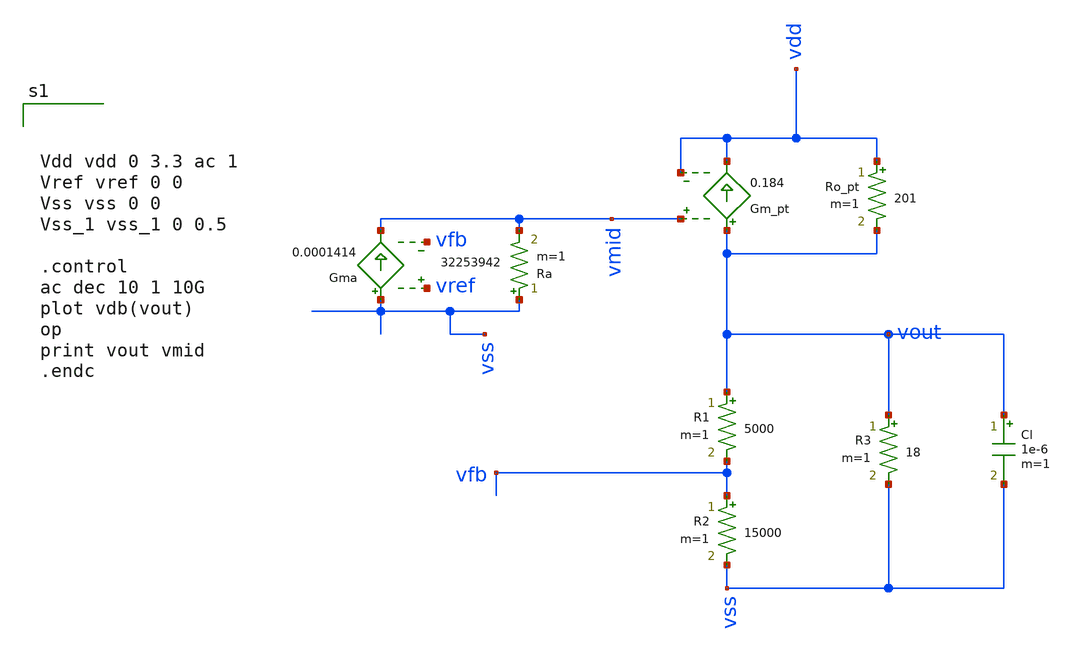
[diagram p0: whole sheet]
** sch_path: test/sstadex/xschem/ldo_tb.sch
**.subckt ldo_tb
Ro_pt vdd vout 201 m=1
Gm_pt vout vdd vmid vdd 0.184
R1 vout vfb 5000 m=1
R2 vfb vss 15000 m=1
Gma vss vmid vref vfb 0.0001414
Ra vss vmid 32253942 m=1
Cl vout vss 1e-6 m=1
R3 vout vss 18 m=1
**** begin user architecture code



Vdd vdd 0 3.3 ac 1
Vref vref 0 0
Vss vss 0 0
Vss_1 vss_1 0 0.5

.control
ac dec 10 1 10G
plot vdb(vout)
op
print vout vmid
.endc



**** end user architecture code
**.ends
.end
